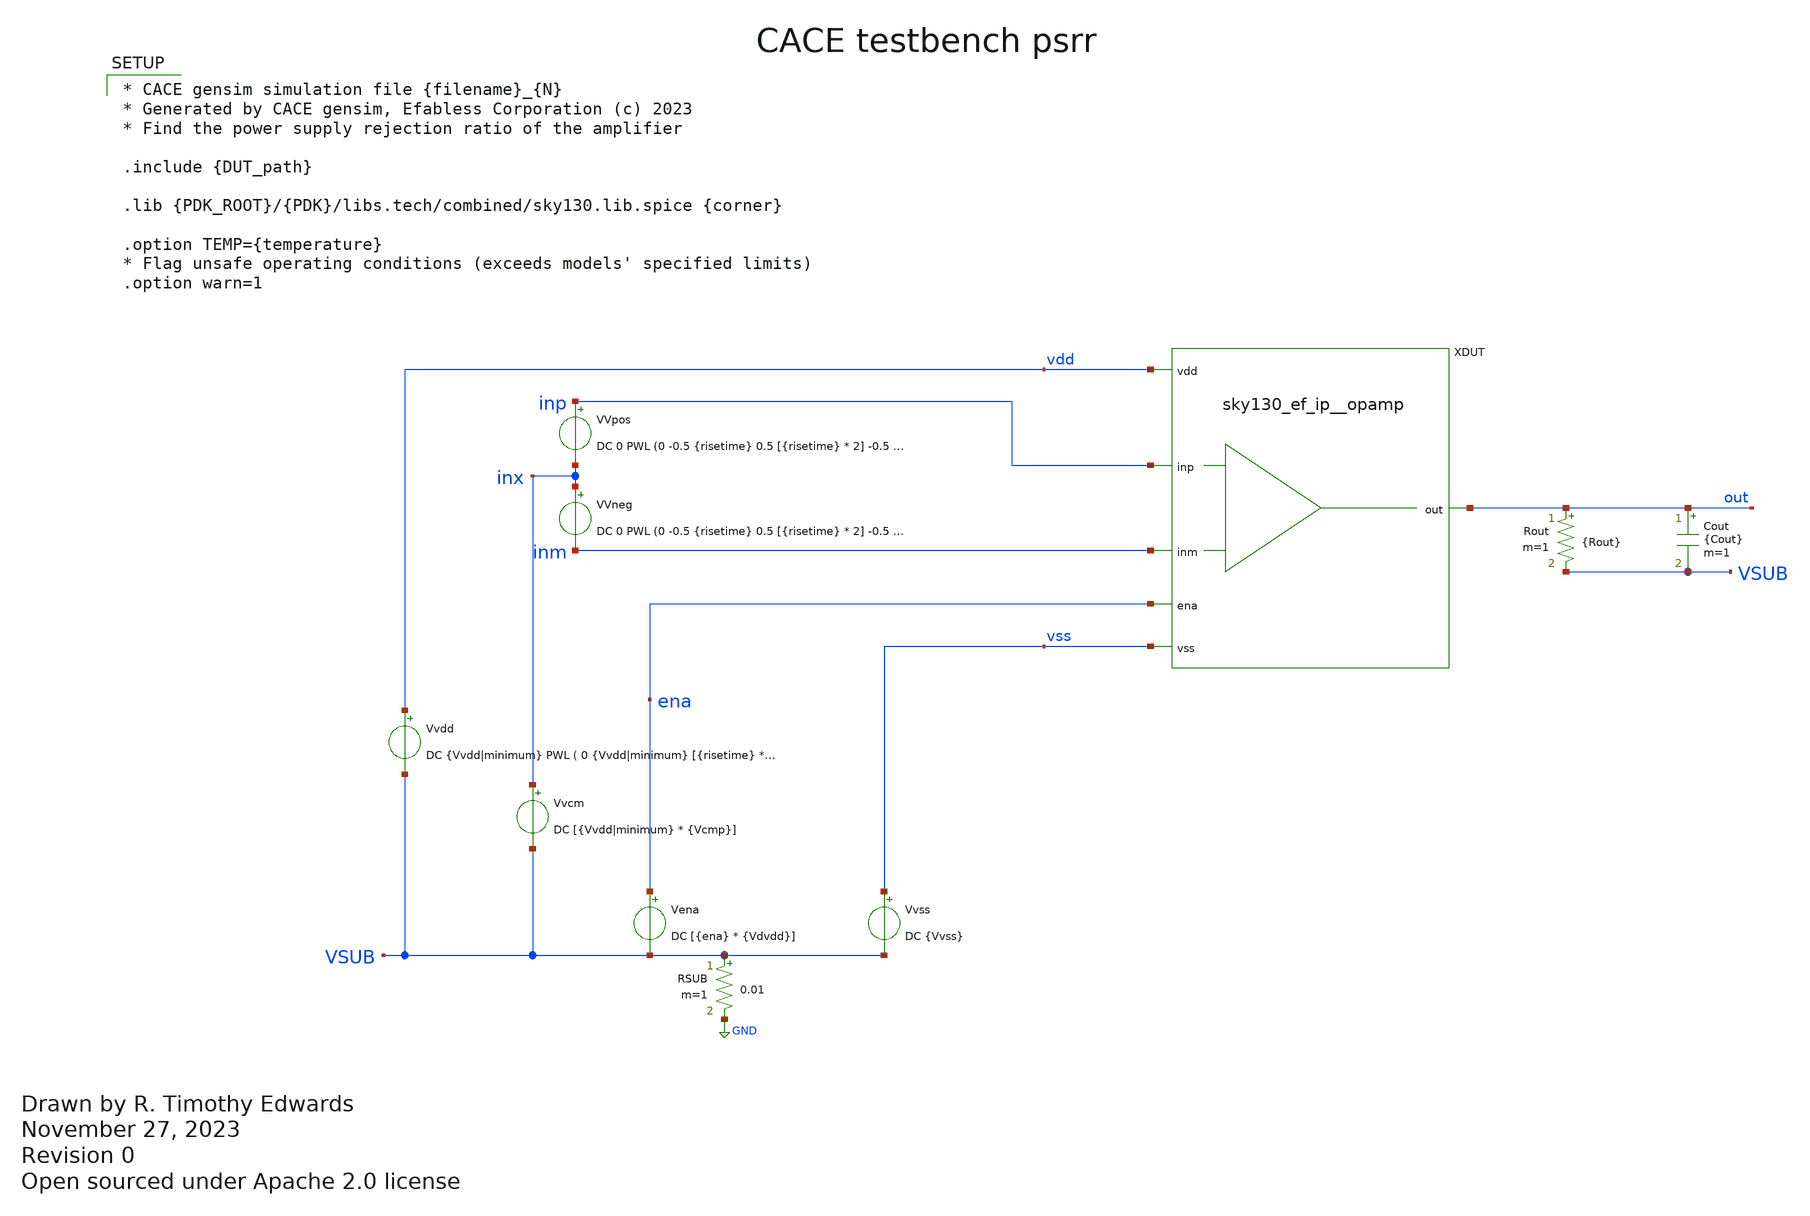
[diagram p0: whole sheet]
** sch_path: cace/templates/psrr.sch
* Open sourced under Apache 2.0 license
**.subckt psrr
Vvdd vdd VSUB DC {Vvdd|minimum} PWL ( 0 {Vvdd|minimum} [{risetime} * 2] {Vvdd|minimum} [{risetime} *
+ 2 + 1e-9] {Vvdd|maximum} [{risetime} * 3] {Vvdd|maximum} )
Vena ena VSUB DC [{ena} * {Vdvdd}]
Vvss vss VSUB DC {Vvss}
Rout out VSUB {Rout} m=1
Cout out VSUB {Cout} m=1
Vvcm inx VSUB DC [{Vvdd|minimum} * {Vcmp}]
RSUB VSUB GND 0.01 m=1
XDUT vdd out ena vss inp inm sky130_ef_ip__opamp
VVpos inp inx DC 0 PWL (0 -0.5 {risetime} 0.5 [{risetime} * 2] -0.5 [{risetime} * 3] 0.5 [{risetime}
+ * 4] -0.5 )
VVneg inx inm DC 0 PWL (0 -0.5 {risetime} 0.5 [{risetime} * 2] -0.5 [{risetime} * 3] 0.5 [{risetime}
+ * 4] -0.5 )
**** begin user architecture code

.control
** PSRR is defined as the change in input offset vs. change in power supply.
tran [{risetime} * 2 / 100] [{risetime} * 4]
meas tran vhigh1 FIND V(inp) WHEN V(out) = [{Vvdd|minimum} / 2] CROSS=1
meas tran vlow1 FIND V(inp) WHEN V(out) = [{Vvdd|minimum} / 2] CROSS=2
meas tran vhigh2 FIND V(inp) WHEN V(out) = [{Vvdd|maximum} / 2] CROSS=3
meas tran vlow2 FIND V(inp) WHEN V(out) = [{Vvdd|maximum} / 2] CROSS=4

let voffset1 = 0.5 * ($&vhigh1 + $&vlow1)
let voffset2 = 0.5 * ($&vhigh2 + $&vlow2)

let psrr = ($&voffset1 - $&voffset2) / ({Vvdd|maximum} - {Vvdd|minimum})
let psrrdb = 20 * log(abs($&psrr))

echo $&psrrdb > {simpath}/{filename}_{N}.data
quit
.endc



* CACE gensim simulation file {filename}_{N}
* Generated by CACE gensim, Efabless Corporation (c) 2023
* Find the power supply rejection ratio of the amplifier

.include {DUT_path}

.lib {PDK_ROOT}/{PDK}/libs.tech/combined/sky130.lib.spice {corner}

.option TEMP={temperature}
* Flag unsafe operating conditions (exceeds models' specified limits)
.option warn=1


**** end user architecture code
**.ends

* expanding   symbol:  sky130_ef_ip__opamp.sym # of pins=6
** sym_path: xschem/sky130_ef_ip__opamp.sym
** sch_path: xschem/sky130_ef_ip__opamp.sch
.subckt sky130_ef_ip__opamp vdd out ena vss inp inm
*.ipin inp
*.ipin vdd
*.ipin vss
*.opin out
*.ipin ena
*.ipin inm
XM4 pdrv1 net1 vdd vdd sky130_fd_pr__pfet_g5v0d10v5 L=0.5 W=2 nf=2 ad='int((nf+1)/2) * W/nf * 0.29' as='int((nf+2)/2)
+ * W/nf * 0.29' pd='2*int((nf+1)/2) * (W/nf + 0.29)' ps='2*int((nf+2)/2) * (W/nf + 0.29)' nrd='0.29 /
+ W' nrs='0.29 / W' sa=0 sb=0 sd=0 mult=1 m=1
XM5 vdd net1 net1 vdd sky130_fd_pr__pfet_g5v0d10v5 L=0.5 W=2 nf=2 ad='int((nf+1)/2) * W/nf * 0.29' as='int((nf+2)/2)
+ * W/nf * 0.29' pd='2*int((nf+1)/2) * (W/nf + 0.29)' ps='2*int((nf+2)/2) * (W/nf + 0.29)' nrd='0.29 /
+ W' nrs='0.29 / W' sa=0 sb=0 sd=0 mult=1 m=1
XM9 vcomn1 nbias vss vss sky130_fd_pr__nfet_g5v0d10v5 L=0.5 W=1 nf=1 ad='int((nf+1)/2) * W/nf * 0.29' as='int((nf+2)/2)
+ * W/nf * 0.29' pd='2*int((nf+1)/2) * (W/nf + 0.29)' ps='2*int((nf+2)/2) * (W/nf + 0.29)' nrd='0.29 /
+ W' nrs='0.29 / W' sa=0 sb=0 sd=0 mult=1 m=1
XM10 vss nbias nbias vss sky130_fd_pr__nfet_g5v0d10v5 L=0.5 W=4 nf=4 ad='int((nf+1)/2) * W/nf * 0.29' as='int((nf+2)/2)
+ * W/nf * 0.29' pd='2*int((nf+1)/2) * (W/nf + 0.29)' ps='2*int((nf+2)/2) * (W/nf + 0.29)' nrd='0.29 /
+ W' nrs='0.29 / W' sa=0 sb=0 sd=0 mult=1 m=1
XR1 net4 vdd vss sky130_fd_pr__res_xhigh_po_0p35 L=100 mult=1 m=1
XM20 out pdrv1 vdd vdd sky130_fd_pr__pfet_g5v0d10v5 L=0.5 W=200 nf=200 ad='int((nf+1)/2) * W/nf * 0.29' as='int((nf+2)/2)
+ * W/nf * 0.29' pd='2*int((nf+1)/2) * (W/nf + 0.29)' ps='2*int((nf+2)/2) * (W/nf + 0.29)' nrd='0.29 /
+ W' nrs='0.29 / W' sa=0 sb=0 sd=0 mult=1 m=1
XM22 out ndrv vss vss sky130_fd_pr__nfet_g5v0d10v5 L=0.5 W=120 nf=120 ad='int((nf+1)/2) * W/nf * 0.29' as='int((nf+2)/2)
+ * W/nf * 0.29' pd='2*int((nf+1)/2) * (W/nf + 0.29)' ps='2*int((nf+2)/2) * (W/nf + 0.29)' nrd='0.29 /
+ W' nrs='0.29 / W' sa=0 sb=0 sd=0 mult=1 m=1
XM24 pbias nbias vss vss sky130_fd_pr__nfet_g5v0d10v5 L=0.5 W=1 nf=1 ad='int((nf+1)/2) * W/nf * 0.29' as='int((nf+2)/2)
+ * W/nf * 0.29' pd='2*int((nf+1)/2) * (W/nf + 0.29)' ps='2*int((nf+2)/2) * (W/nf + 0.29)' nrd='0.29 /
+ W' nrs='0.29 / W' sa=0 sb=0 sd=0 mult=1 m=1
XM25 vdd pbias pbias vdd sky130_fd_pr__pfet_g5v0d10v5 L=0.5 W=1 nf=1 ad='int((nf+1)/2) * W/nf * 0.29' as='int((nf+2)/2)
+ * W/nf * 0.29' pd='2*int((nf+1)/2) * (W/nf + 0.29)' ps='2*int((nf+2)/2) * (W/nf + 0.29)' nrd='0.29 /
+ W' nrs='0.29 / W' sa=0 sb=0 sd=0 mult=1 m=1
XM26 vcomp pbias vdd vdd sky130_fd_pr__pfet_g5v0d10v5 L=0.5 W=2 nf=2 ad='int((nf+1)/2) * W/nf * 0.29' as='int((nf+2)/2)
+ * W/nf * 0.29' pd='2*int((nf+1)/2) * (W/nf + 0.29)' ps='2*int((nf+2)/2) * (W/nf + 0.29)' nrd='0.29 /
+ W' nrs='0.29 / W' sa=0 sb=0 sd=0 mult=1 m=1
XM27 net2 inm vcomp vdd sky130_fd_pr__pfet_g5v0d10v5 L=0.5 W=2 nf=2 ad='int((nf+1)/2) * W/nf * 0.29' as='int((nf+2)/2)
+ * W/nf * 0.29' pd='2*int((nf+1)/2) * (W/nf + 0.29)' ps='2*int((nf+2)/2) * (W/nf + 0.29)' nrd='0.29 /
+ W' nrs='0.29 / W' sa=0 sb=0 sd=0 mult=1 m=1
XM28 vcomp inp ndrv vdd sky130_fd_pr__pfet_g5v0d10v5 L=0.5 W=2 nf=2 ad='int((nf+1)/2) * W/nf * 0.29' as='int((nf+2)/2)
+ * W/nf * 0.29' pd='2*int((nf+1)/2) * (W/nf + 0.29)' ps='2*int((nf+2)/2) * (W/nf + 0.29)' nrd='0.29 /
+ W' nrs='0.29 / W' sa=0 sb=0 sd=0 mult=1 m=1
XM29 ndrv net2 vss vss sky130_fd_pr__nfet_g5v0d10v5 L=0.5 W=1 nf=1 ad='int((nf+1)/2) * W/nf * 0.29' as='int((nf+2)/2)
+ * W/nf * 0.29' pd='2*int((nf+1)/2) * (W/nf + 0.29)' ps='2*int((nf+2)/2) * (W/nf + 0.29)' nrd='0.29 /
+ W' nrs='0.29 / W' sa=0 sb=0 sd=0 mult=1 m=1
XM30 vss net2 net2 vss sky130_fd_pr__nfet_g5v0d10v5 L=0.5 W=1 nf=1 ad='int((nf+1)/2) * W/nf * 0.29' as='int((nf+2)/2)
+ * W/nf * 0.29' pd='2*int((nf+1)/2) * (W/nf + 0.29)' ps='2*int((nf+2)/2) * (W/nf + 0.29)' nrd='0.29 /
+ W' nrs='0.29 / W' sa=0 sb=0 sd=0 mult=1 m=1
XM1 net1 inm vcomn1 vss sky130_fd_pr__nfet_g5v0d10v5 L=0.5 W=1 nf=1 ad='int((nf+1)/2) * W/nf * 0.29' as='int((nf+2)/2)
+ * W/nf * 0.29' pd='2*int((nf+1)/2) * (W/nf + 0.29)' ps='2*int((nf+2)/2) * (W/nf + 0.29)' nrd='0.29 /
+ W' nrs='0.29 / W' sa=0 sb=0 sd=0 mult=1 m=1
XM2 vcomn1 inp pdrv1 vss sky130_fd_pr__nfet_g5v0d10v5 L=0.5 W=1 nf=1 ad='int((nf+1)/2) * W/nf * 0.29' as='int((nf+2)/2)
+ * W/nf * 0.29' pd='2*int((nf+1)/2) * (W/nf + 0.29)' ps='2*int((nf+2)/2) * (W/nf + 0.29)' nrd='0.29 /
+ W' nrs='0.29 / W' sa=0 sb=0 sd=0 mult=1 m=1
XM3 pdrv2 net3 vdd vdd sky130_fd_pr__pfet_g5v0d10v5 L=0.5 W=2 nf=2 ad='int((nf+1)/2) * W/nf * 0.29' as='int((nf+2)/2)
+ * W/nf * 0.29' pd='2*int((nf+1)/2) * (W/nf + 0.29)' ps='2*int((nf+2)/2) * (W/nf + 0.29)' nrd='0.29 /
+ W' nrs='0.29 / W' sa=0 sb=0 sd=0 mult=1 m=1
XM6 vdd net3 net3 vdd sky130_fd_pr__pfet_g5v0d10v5 L=0.5 W=2 nf=2 ad='int((nf+1)/2) * W/nf * 0.29' as='int((nf+2)/2)
+ * W/nf * 0.29' pd='2*int((nf+1)/2) * (W/nf + 0.29)' ps='2*int((nf+2)/2) * (W/nf + 0.29)' nrd='0.29 /
+ W' nrs='0.29 / W' sa=0 sb=0 sd=0 mult=1 m=1
XM7 vcomn2 nbias vss vss sky130_fd_pr__nfet_g5v0d10v5 L=0.5 W=1 nf=1 ad='int((nf+1)/2) * W/nf * 0.29' as='int((nf+2)/2)
+ * W/nf * 0.29' pd='2*int((nf+1)/2) * (W/nf + 0.29)' ps='2*int((nf+2)/2) * (W/nf + 0.29)' nrd='0.29 /
+ W' nrs='0.29 / W' sa=0 sb=0 sd=0 mult=1 m=1
XM8 net3 inm vcomn2 vss sky130_fd_pr__nfet_03v3_nvt L=0.5 W=1 nf=1 ad='int((nf+1)/2) * W/nf * 0.29' as='int((nf+2)/2)
+ * W/nf * 0.29' pd='2*int((nf+1)/2) * (W/nf + 0.29)' ps='2*int((nf+2)/2) * (W/nf + 0.29)' nrd='0.29 /
+ W' nrs='0.29 / W' sa=0 sb=0 sd=0 mult=1 m=1
XM11 vcomn2 inp pdrv2 vss sky130_fd_pr__nfet_03v3_nvt L=0.5 W=1 nf=1 ad='int((nf+1)/2) * W/nf * 0.29' as='int((nf+2)/2)
+ * W/nf * 0.29' pd='2*int((nf+1)/2) * (W/nf + 0.29)' ps='2*int((nf+2)/2) * (W/nf + 0.29)' nrd='0.29 /
+ W' nrs='0.29 / W' sa=0 sb=0 sd=0 mult=1 m=1
XM12 vdd pdrv2 out vdd sky130_fd_pr__pfet_g5v0d10v5 L=0.5 W=200 nf=200 ad='int((nf+1)/2) * W/nf * 0.29' as='int((nf+2)/2)
+ * W/nf * 0.29' pd='2*int((nf+1)/2) * (W/nf + 0.29)' ps='2*int((nf+2)/2) * (W/nf + 0.29)' nrd='0.29 /
+ W' nrs='0.29 / W' sa=0 sb=0 sd=0 mult=1 m=1
XXD1 vss inp sky130_fd_pr__diode_pw2nd_05v5 area=3.6e11 pj=4e6
XM13 net4 ena nbias vss sky130_fd_pr__nfet_g5v0d10v5 L=0.5 W=1 nf=1 ad='int((nf+1)/2) * W/nf * 0.29' as='int((nf+2)/2)
+ * W/nf * 0.29' pd='2*int((nf+1)/2) * (W/nf + 0.29)' ps='2*int((nf+2)/2) * (W/nf + 0.29)' nrd='0.29 /
+ W' nrs='0.29 / W' sa=0 sb=0 sd=0 mult=1 m=1
XXD2 vss ena sky130_fd_pr__diode_pw2nd_05v5 area=3.6e11 pj=4e6
XXD3 vss inm sky130_fd_pr__diode_pw2nd_05v5 area=3.6e11 pj=4e6
.ends

.GLOBAL GND
.end
